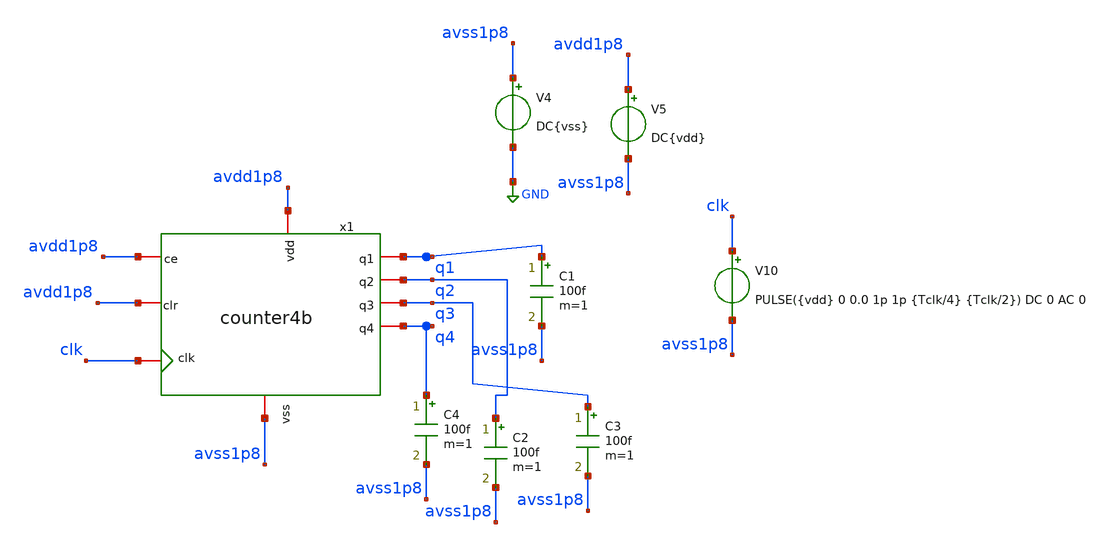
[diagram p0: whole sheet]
** sch_path: verification/testbenches/counter4b_ed/tb_counter4b.sch
**.subckt tb_counter4b
x1 avdd1p8 avss1p8 q1 avdd1p8 avdd1p8 clk q2 q3 q4 counter4b
V4 avss1p8 GND DC{vss}
V10 clk avss1p8 PULSE({vdd} 0 0.0 1p 1p {Tclk/4} {Tclk/2}) DC 0 AC 0
V5 avdd1p8 avss1p8 DC{vdd}
C1 q1 avss1p8 100f m=1
C2 q2 avss1p8 100f m=1
C3 q3 avss1p8 100f m=1
C4 q4 avss1p8 100f m=1
**** begin user architecture code


* Circuit Parameters
.param vdd = 1.2
.param vss = 0.0
.param Tclk = 10n
.param Tffd = 85n
.param Tclear = 165n
.options TEMP = 27.0
* Include Models - IHP SG13G2
.lib cornerMOSlv.lib mos_tt
* OP Parameters & Singals to save
.save all
*Simulations
.control
tran 0.01u 200n
setplot tran1
plot v(clk) v(q1)+2.4 v(q2)+3.6 v(q3)+4.8 v(q4)+6.0
reset
dc V6 0 1.2 0.01
setplot dc
plot vin vout ylabel vout xlabel vin
set filetype = ascii
write dcsweep.raw
.endc
.end


**** end user architecture code
**.ends
.GLOBAL GND
.end
